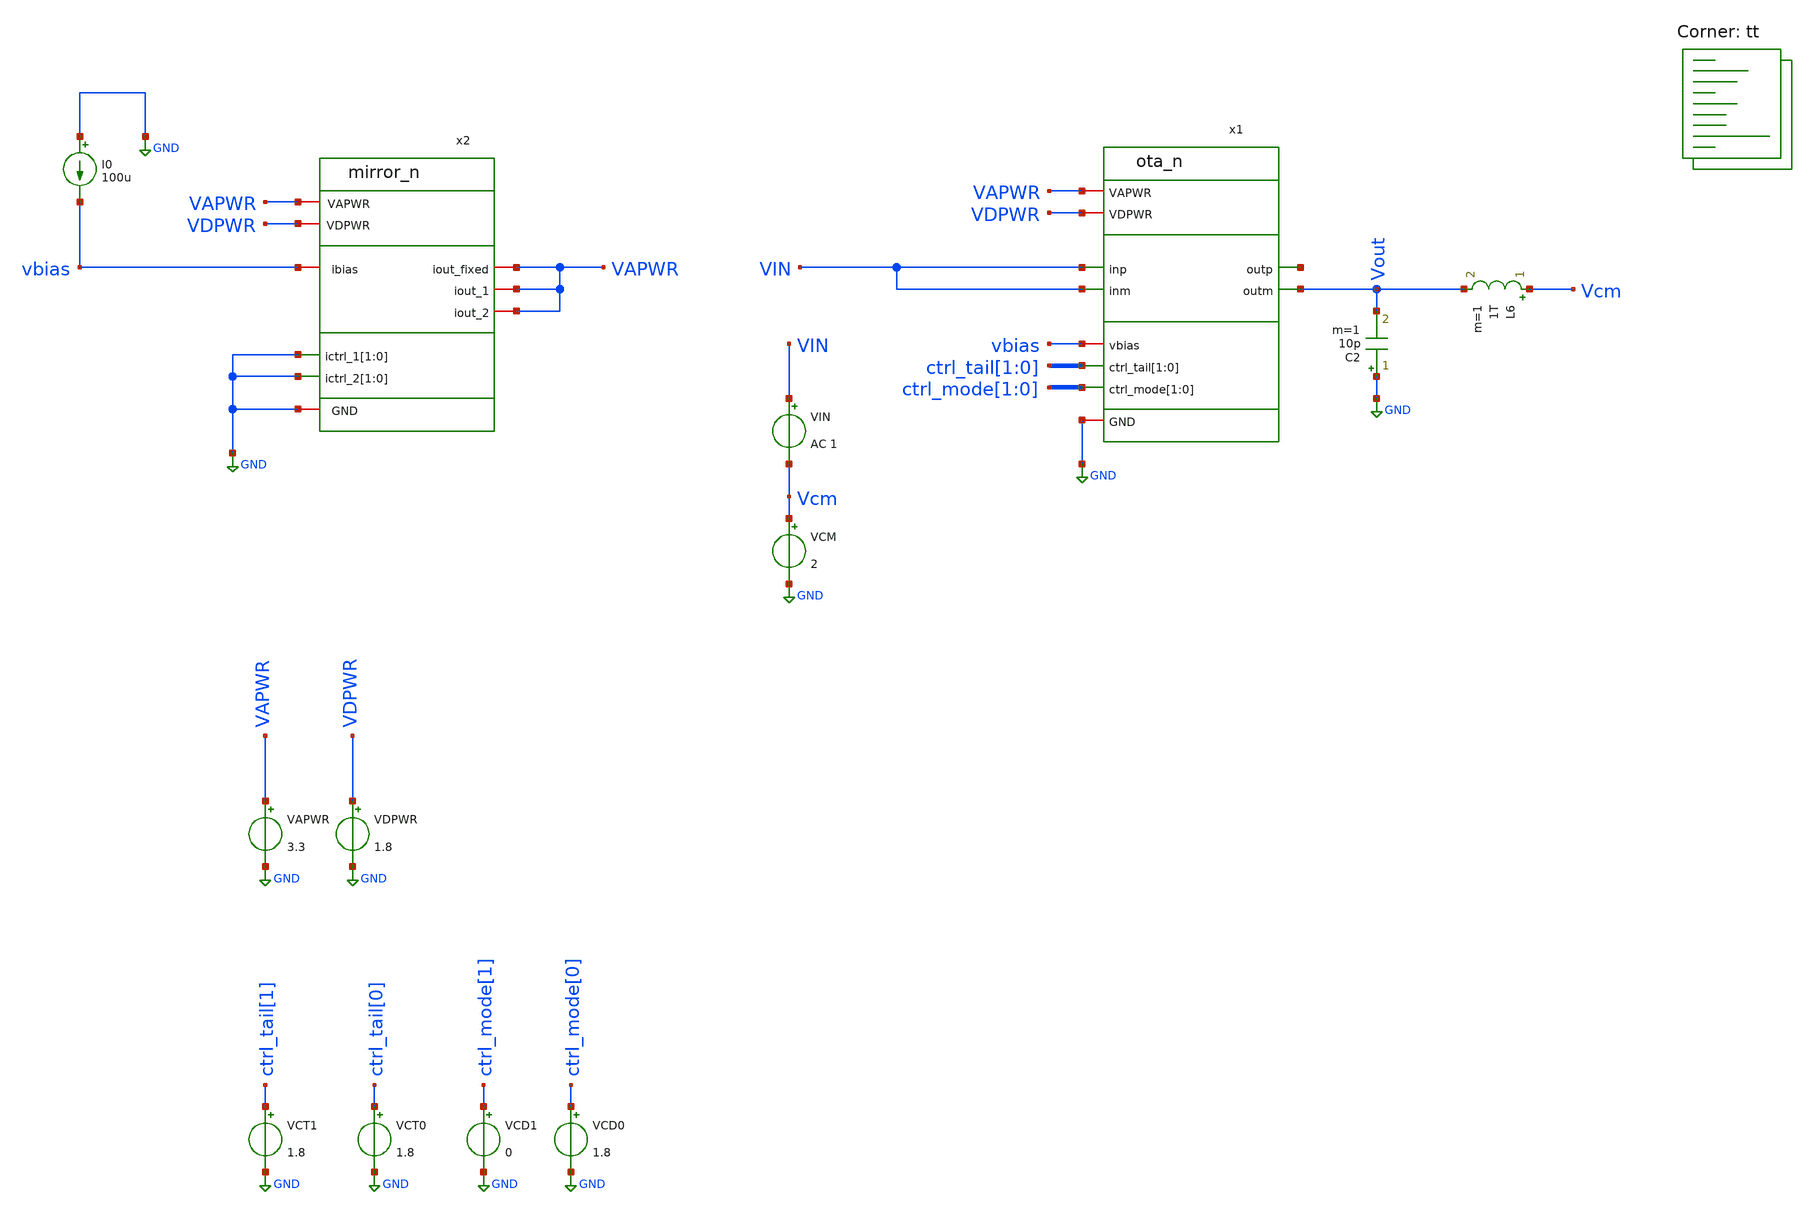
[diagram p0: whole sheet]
** sch_path: xschem/tb_ota_n_cmrr.sch
**.subckt tb_ota_n_cmrr
x1 VAPWR VDPWR VIN net1 VIN ctrl_tail[1] ctrl_tail[0] ctrl_mode[1] ctrl_mode[0] vbias GND Vout ota_n
VAPWR VAPWR GND 3.3
VDPWR VDPWR GND 1.8
x2 VAPWR VDPWR vbias VAPWR VAPWR VAPWR GND GND GND GND GND mirror_n
I0 GND vbias 100u
VCM Vcm GND 2
VCT1 ctrl_tail[1] GND 1.8
VCT0 ctrl_tail[0] GND 1.8
VCD1 ctrl_mode[1] GND 0
VIN VIN Vcm AC 1
L6 Vcm Vout 1T m=1
C2 GND Vout 10p m=1
VCD0 ctrl_mode[0] GND 1.8
**** begin user architecture code
.lib $::SKYWATER_MODELS/sky130.lib.spice tt


*****************************************
* OTA CMRR Test
*****************************************
* plots the CMR of the 5T OTA for various tail currents
*****************************************
.control
   save all
   set temp = 27
   set wr_singlescale
   set wr_vecnames
   alter VCM 2
   alter VCT1 0
   alter VCT0 0
   repeat 2
      repeat 2
         ac dec 51 10k 10G
         alter VCT0 1.8
      end
      alter VCT1 1.8
      alter VCT0 0
   end
   plot vdb(ac1.v(Vout)) vdb(ac2.v(Vout)) vdb(ac3.v(Vout)) vdb(ac4.v(Vout))
*   plot ph(ac1.v(Vout))/PI*180 ph(ac2.v(Vout))/PI*180 ph(ac3.v(Vout))/PI*180 ph(ac4.v(Vout))/PI*180
.endc


**** end user architecture code
**.ends
.GLOBAL GND
.end
